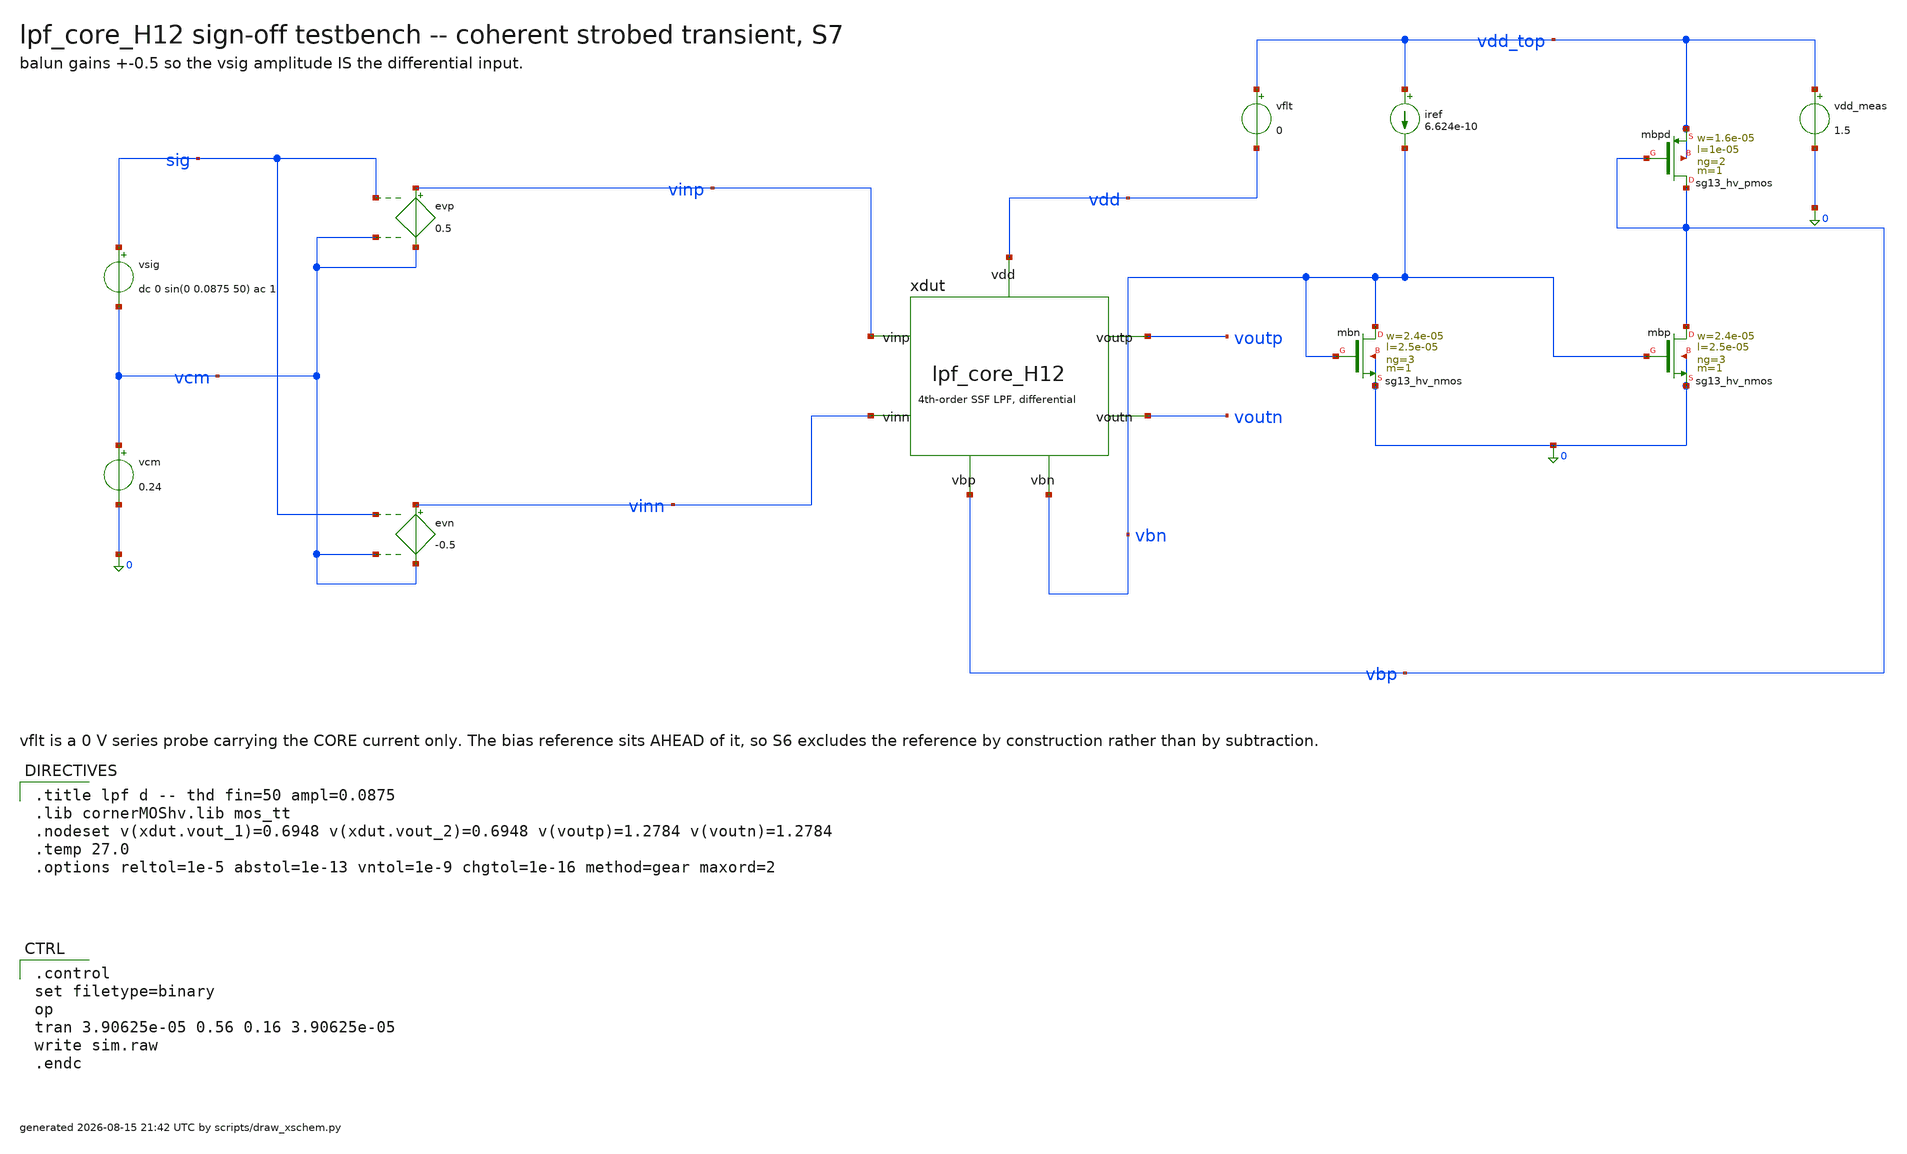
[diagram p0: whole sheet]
** sch_path: signoff/post-pvt/H12-robust/lpf_tb_H12_thd.sch
**.subckt lpf_tb_H12_thd
vsig sig vcm dc 0 sin(0 0.0875 50) ac 1
vcm vcm 0 0.24
evp vinp vcm sig vcm 0.5
evn vinn vcm sig vcm -0.5
xdut vinp vinn voutp voutn vbn vbp vdd lpf_core_H12
vflt vdd_top vdd 0
vdd_meas vdd_top 0 1.5
iref vdd_top vbn 6.624e-10
Xmbn vbn vbn 0 0 sg13_hv_nmos w=2.4e-05 l=2.5e-05 ng=3 m=1 mm_ok=1
Xmbp vbp vbn 0 0 sg13_hv_nmos w=2.4e-05 l=2.5e-05 ng=3 m=1 mm_ok=1
Xmbpd vbp vbp vdd_top vdd_top sg13_hv_pmos w=1.6e-05 l=1e-05 ng=2 m=1 mm_ok=1
**** begin user architecture code

.title lpf d -- thd fin=50 ampl=0.0875
.lib cornerMOShv.lib mos_tt
.nodeset v(xdut.vout_1)=0.6948 v(xdut.vout_2)=0.6948 v(voutp)=1.2784 v(voutn)=1.2784
.temp 27.0
.options reltol=1e-5 abstol=1e-13 vntol=1e-9 chgtol=1e-16 method=gear maxord=2


.control
set filetype=binary
op
tran 3.90625e-05 0.56 0.16 3.90625e-05
write sim.raw
.endc

**** end user architecture code
**.ends

* expanding   symbol:  lpf_core_H12.sym # of pins=7
** sym_path: signoff/post-pvt/H12-robust/lpf_core_H12.sym
** sch_path: signoff/post-pvt/H12-robust/lpf_core_H12.sch
.subckt lpf_core_H12 vinp vinn voutp voutn vbn vbp vdd
*.ipin vinp
*.ipin vinn
*.opin voutp
*.opin voutn
*.ipin vdd
*.ipin vbn
*.ipin vbp
Xm2 net2 vinp vout_1 vout_1 sg13_hv_pmos w=1.6e-05 l=1e-05 ng=2 m=1 mm_ok=1
Xm5 net3 vinn vout_2 vout_2 sg13_hv_pmos w=1.6e-05 l=1e-05 ng=2 m=1 mm_ok=1
Xm4 vout_1 net2 0 0 sg13_hv_nmos w=1.5e-06 l=4.5e-05 ng=1 m=1 mm_ok=1
Xm8 vout_2 net3 0 0 sg13_hv_nmos w=1.5e-06 l=4.5e-05 ng=1 m=1 mm_ok=1
Xm9 net2 vbn 0 0 sg13_hv_nmos w=2.4e-05 l=2.5e-05 ng=3 m=1 mm_ok=1
Xm10 net3 vbn 0 0 sg13_hv_nmos w=2.4e-05 l=2.5e-05 ng=3 m=1 mm_ok=1
Xmst vout_1 vbr net4 net4 sg13_hv_pmos w=5e-06 l=3.3e-05 ng=1 m=1 mm_ok=1
Xmstn vout_2 vbr net1 net1 sg13_hv_pmos w=5e-06 l=3.3e-05 ng=1 m=1 mm_ok=1
Xm0 net4 vout_1 voutp voutp sg13_hv_pmos w=4e-06 l=1.5e-05 ng=1 m=1 mm_ok=1
Xm1 net1 vout_2 voutn voutn sg13_hv_pmos w=4e-06 l=1.5e-05 ng=1 m=1 mm_ok=1
Xm14 voutp net4 vdd vdd sg13_hv_pmos w=1.2e-05 l=3.1e-05 ng=2 m=1 mm_ok=1
Xm15 voutn net1 vdd vdd sg13_hv_pmos w=1.2e-05 l=3.1e-05 ng=2 m=1 mm_ok=1
Xr1 rep_x rep_x vdd vdd sg13_hv_pmos w=1.2e-05 l=3.1e-05 ng=2 m=1 mm_ok=1
Xr2 vbr vbr rep_x rep_x sg13_hv_pmos w=5e-06 l=3.3e-05 ng=1 m=1 mm_ok=1
Xr3 vbr vbn 0 0 sg13_hv_nmos w=2.4e-05 l=2.5e-05 ng=3 m=4 mm_ok=1
c13 net2 vout_1 4.95e-12 m=1
c17 net3 vout_2 4.95e-12 m=1
c19 vout_2 vout_1 2.931e-11 m=1
c1 voutp net4 5.998e-11 m=1
c10 voutn net1 5.998e-11 m=1
c12 voutn voutp 2.456e-11 m=1
.ends

.end
